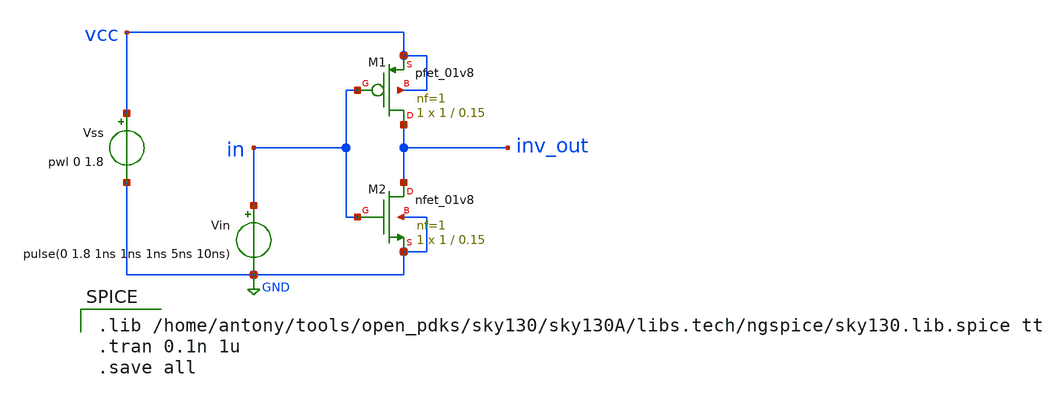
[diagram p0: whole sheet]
** sch_path: inverter130/inverter130_schematic.sch
**.subckt inverter130_schematic
Vss vcc GND pwl 0 1.8
Vin in GND pulse(0 1.8 1ns 1ns 1ns 5ns 10ns)
XM1 inv_out in vcc vcc sky130_fd_pr__pfet_01v8 L=0.15 W=1 nf=1 ad='int((nf+1)/2) * W/nf * 0.29' as='int((nf+2)/2) * W/nf * 0.29'
+ pd='2*int((nf+1)/2) * (W/nf + 0.29)' ps='2*int((nf+2)/2) * (W/nf + 0.29)' nrd='0.29 / W' nrs='0.29 / W'
+ sa=0 sb=0 sd=0 mult=1 m=1
XM2 inv_out in GND GND sky130_fd_pr__nfet_01v8 L=0.15 W=1 nf=1 ad='int((nf+1)/2) * W/nf * 0.29' as='int((nf+2)/2) * W/nf * 0.29'
+ pd='2*int((nf+1)/2) * (W/nf + 0.29)' ps='2*int((nf+2)/2) * (W/nf + 0.29)' nrd='0.29 / W' nrs='0.29 / W'
+ sa=0 sb=0 sd=0 mult=1 m=1
**** begin user architecture code

.lib /home/antony/tools/open_pdks/sky130/sky130A/libs.tech/ngspice/sky130.lib.spice tt
.tran 0.1n 1u
.save all

**** end user architecture code
**.ends
.GLOBAL GND
.end
